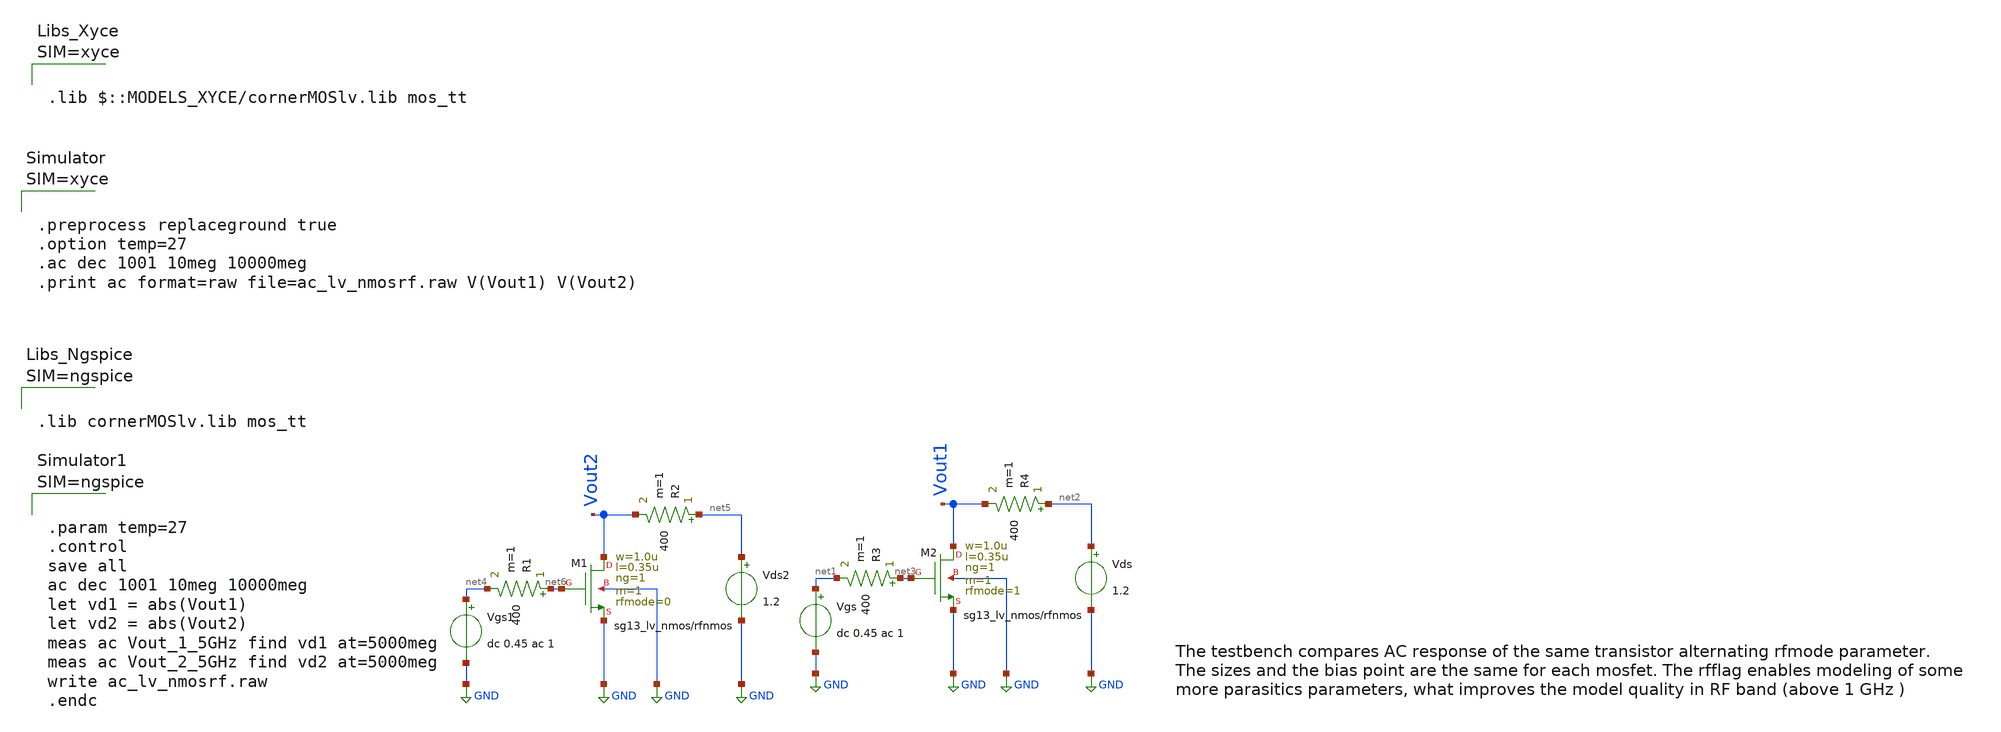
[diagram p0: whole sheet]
** sch_path: ihp-sg13g2/libs.tech/xschem/sg13g2_tests_xyce/ac_lv_nmosrf.sch
* Copyright 2023 IHP PDK Authors
**.subckt ac_lv_nmosrf
Vgs net1 GND dc 0.45 ac 1
Vds net2 GND 1.2
Vgs1 net4 GND dc 0.45 ac 1
Vds2 net5 GND 1.2
XM1 Vout2 net6 GND GND sg13_lv_nmos w=1.0u l=0.35u ng=1 m=1 rfmode=0 mm_ok=1
XM2 Vout1 net3 GND GND sg13_lv_nmos w=1.0u l=0.35u ng=1 m=1 rfmode=1 mm_ok=1
R1 net6 net4 400 m=1
R2 net5 Vout2 400 m=1
R3 net3 net1 400 m=1
R4 net2 Vout1 400 m=1
**** begin user architecture code









.lib cornerMOSlv.lib mos_tt






.param temp=27
.control
save all
ac dec 1001 10meg 10000meg
let vd1 = abs(Vout1)
let vd2 = abs(Vout2)
meas ac Vout_1_5GHz find vd1 at=5000meg
meas ac Vout_2_5GHz find vd2 at=5000meg
write ac_lv_nmosrf.raw
.endc



**** end user architecture code
**.ends
.GLOBAL GND
.end
